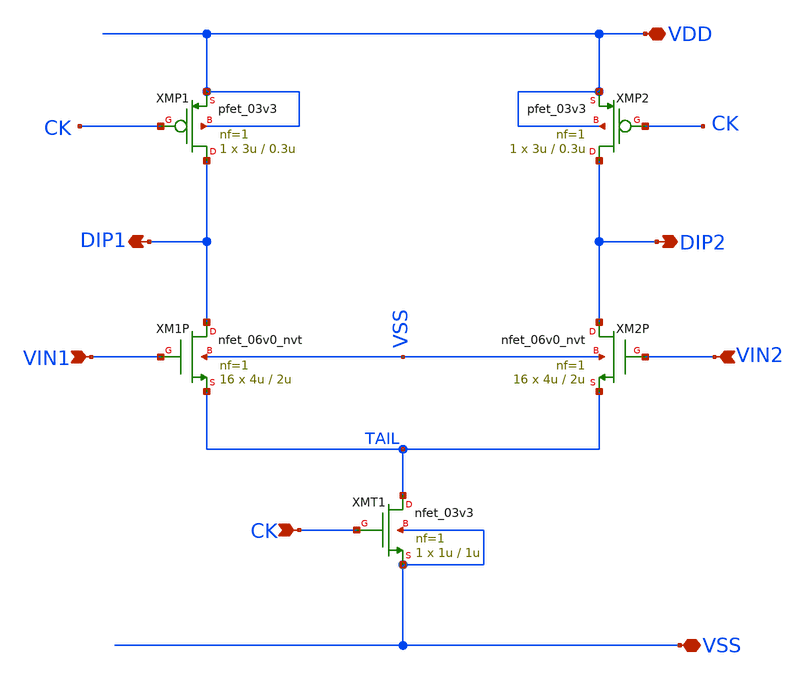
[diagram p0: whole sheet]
** sch_path: comparator_alt/schematic/preamp_dyn.sch
**.subckt preamp_dyn VIN1 VIN2 VDD VSS DIP1 DIP2 CK
*.ipin VIN1
*.ipin VIN2
*.iopin VDD
*.iopin VSS
*.opin DIP1
*.opin DIP2
*.ipin CK
XMT1 TAIL CK VSS VSS nfet_03v3 L=1u W=1u nf=1 ad='int((nf+1)/2) * W/nf * 0.18u' as='int((nf+2)/2) * W/nf * 0.18u'
+ pd='2*int((nf+1)/2) * (W/nf + 0.18u)' ps='2*int((nf+2)/2) * (W/nf + 0.18u)' nrd='0.18u / W' nrs='0.18u / W'
+ sa=0 sb=0 sd=0 m=1
XMP1 DIP1 CK VDD VDD pfet_03v3 L=0.3u W=3u nf=1 ad='int((nf+1)/2) * W/nf * 0.18u' as='int((nf+2)/2) * W/nf * 0.18u'
+ pd='2*int((nf+1)/2) * (W/nf + 0.18u)' ps='2*int((nf+2)/2) * (W/nf + 0.18u)' nrd='0.18u / W' nrs='0.18u / W'
+ sa=0 sb=0 sd=0 m=1
XMP2 DIP2 CK VDD VDD pfet_03v3 L=0.3u W=3u nf=1 ad='int((nf+1)/2) * W/nf * 0.18u' as='int((nf+2)/2) * W/nf * 0.18u'
+ pd='2*int((nf+1)/2) * (W/nf + 0.18u)' ps='2*int((nf+2)/2) * (W/nf + 0.18u)' nrd='0.18u / W' nrs='0.18u / W'
+ sa=0 sb=0 sd=0 m=1
XM2P DIP2 VIN2 TAIL VSS nfet_06v0_nvt L=2u W=4u nf=1 ad='int((nf+1)/2) * W/nf * 0.18u' as='int((nf+2)/2) * W/nf * 0.18u'
+ pd='2*int((nf+1)/2) * (W/nf + 0.18u)' ps='2*int((nf+2)/2) * (W/nf + 0.18u)' nrd='0.18u / W' nrs='0.18u / W'
+ sa=0 sb=0 sd=0 m=16
XM1P DIP1 VIN1 TAIL VSS nfet_06v0_nvt L=2u W=4u nf=1 ad='int((nf+1)/2) * W/nf * 0.18u' as='int((nf+2)/2) * W/nf * 0.18u'
+ pd='2*int((nf+1)/2) * (W/nf + 0.18u)' ps='2*int((nf+2)/2) * (W/nf + 0.18u)' nrd='0.18u / W' nrs='0.18u / W'
+ sa=0 sb=0 sd=0 m=16
**.ends
.end
